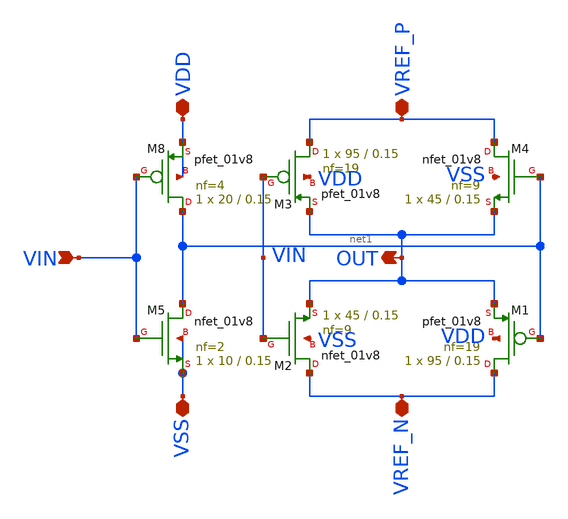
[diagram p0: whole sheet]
** sch_path: DeltaSigma/xschem/1Bit_DAC_Inv.sch
**.subckt 1Bit_DAC_Inv VREF_P VREF_N VSS VDD VIN OUT
*.iopin VREF_P
*.iopin VREF_N
*.iopin VSS
*.iopin VDD
*.ipin VIN
*.opin OUT
XM1 VREF_N net1 OUT VDD sky130_fd_pr__pfet_01v8 L=0.15 W=95 nf=19 ad='int((nf+1)/2) * W/nf * 0.29' as='int((nf+2)/2) * W/nf * 0.29'
+ pd='2*int((nf+1)/2) * (W/nf + 0.29)' ps='2*int((nf+2)/2) * (W/nf + 0.29)' nrd='0.29 / W' nrs='0.29 / W'
+ sa=0 sb=0 sd=0 mult=1 m=1
XM2 VREF_N VIN OUT VSS sky130_fd_pr__nfet_01v8 L=0.15 W=45 nf=9 ad='int((nf+1)/2) * W/nf * 0.29' as='int((nf+2)/2) * W/nf * 0.29'
+ pd='2*int((nf+1)/2) * (W/nf + 0.29)' ps='2*int((nf+2)/2) * (W/nf + 0.29)' nrd='0.29 / W' nrs='0.29 / W'
+ sa=0 sb=0 sd=0 mult=1 m=1
XM3 VREF_P VIN OUT VDD sky130_fd_pr__pfet_01v8 L=0.15 W=95 nf=19 ad='int((nf+1)/2) * W/nf * 0.29' as='int((nf+2)/2) * W/nf * 0.29'
+ pd='2*int((nf+1)/2) * (W/nf + 0.29)' ps='2*int((nf+2)/2) * (W/nf + 0.29)' nrd='0.29 / W' nrs='0.29 / W'
+ sa=0 sb=0 sd=0 mult=1 m=1
XM4 VREF_P net1 OUT VSS sky130_fd_pr__nfet_01v8 L=0.15 W=45 nf=9 ad='int((nf+1)/2) * W/nf * 0.29' as='int((nf+2)/2) * W/nf * 0.29'
+ pd='2*int((nf+1)/2) * (W/nf + 0.29)' ps='2*int((nf+2)/2) * (W/nf + 0.29)' nrd='0.29 / W' nrs='0.29 / W'
+ sa=0 sb=0 sd=0 mult=1 m=1
XM8 net1 VIN VDD VDD sky130_fd_pr__pfet_01v8 L=0.15 W=20 nf=4 ad='W * 0.29' as='W * 0.29' pd='2 * (W + 0.29)'
+ ps='2 * (W + 0.29)' nrd='0.29 / W' nrs='0.29 / W' sa=0 sb=0 sd=0 mult=1 m=1
XM5 net1 VIN VSS VSS sky130_fd_pr__nfet_01v8 L=0.15 W=10 nf=2 ad='int((nf+1)/2) * W/nf * 0.29' as='int((nf+2)/2) * W/nf * 0.29'
+ pd='2*int((nf+1)/2) * (W/nf + 0.29)' ps='2*int((nf+2)/2) * (W/nf + 0.29)' nrd='0.29 / W' nrs='0.29 / W'
+ sa=0 sb=0 sd=0 mult=1 m=1
**.ends
.end
